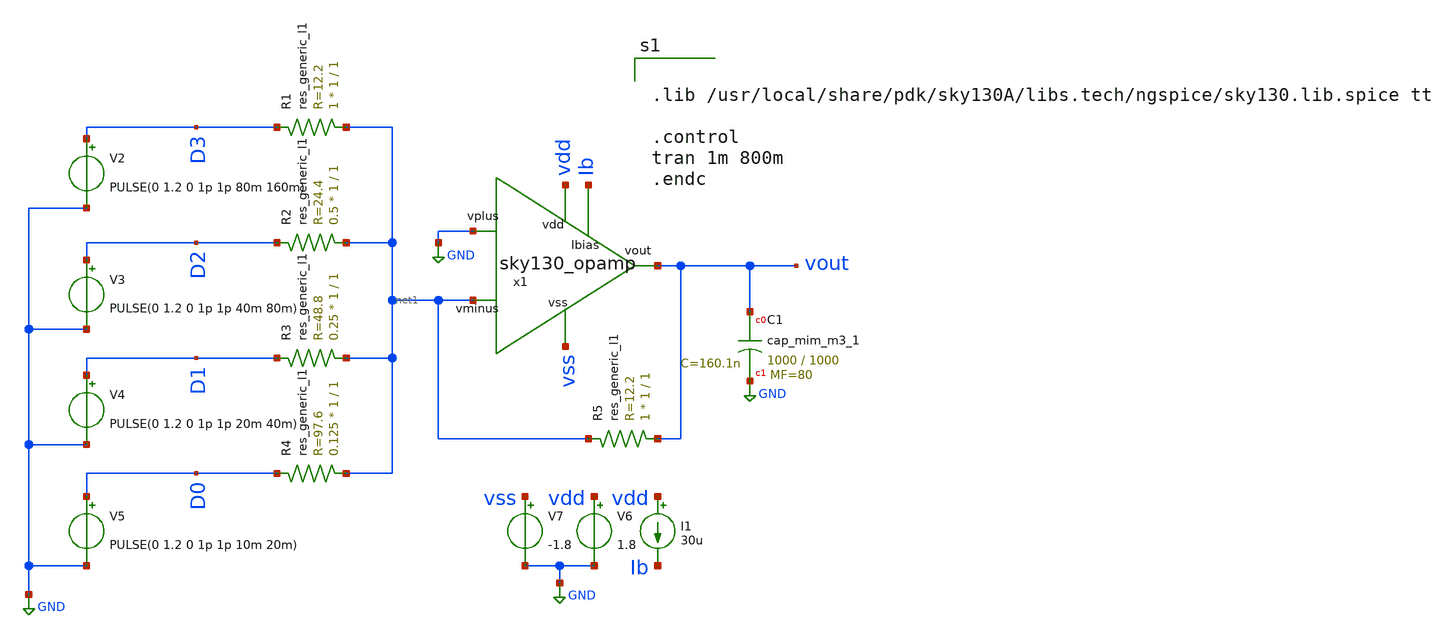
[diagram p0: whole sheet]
** sch_path: Digital to Analog Converter (DAC)/Binary Weighted DAC/binary_weighted_dac.sch
**.subckt binary_weighted_dac
x1 vdd vout GND net1 Ib vss sky130_opamp
R1 net1 D3 sky130_fd_pr__res_generic_l1 W=1 L=1 m=1
R2 net1 D2 sky130_fd_pr__res_generic_l1 W=1 L=1 m=0.5
R3 net1 D1 sky130_fd_pr__res_generic_l1 W=1 L=1 m=0.25
R4 net1 D0 sky130_fd_pr__res_generic_l1 W=1 L=1 m=0.125
V2 D3 GND PULSE(0 1.2 0 1p 1p 80m 160m)
V3 D2 GND PULSE(0 1.2 0 1p 1p 40m 80m)
V4 D1 GND PULSE(0 1.2 0 1p 1p 20m 40m)
V5 D0 GND PULSE(0 1.2 0 1p 1p 10m 20m)
V6 vdd GND 1.8
V7 vss GND -1.8
I1 vdd Ib 30u
R5 vout net1 sky130_fd_pr__res_generic_l1 W=1 L=1 m=1
XC1 vout GND sky130_fd_pr__cap_mim_m3_1 W=1000 L=1000 MF=80 m=80
**** begin user architecture code


.lib /usr/local/share/pdk/sky130A/libs.tech/ngspice/sky130.lib.spice tt

.control
tran 1m 800m
.endc


**** end user architecture code
**.ends

* expanding   symbol:  /home/rachtih/ADC trials/opamp/sky130_opamp.sym # of pins=6
** sym_path: Primitives/Operational Amplifier/Xschem Files/sky130_opamp.sym
** sch_path: Primitives/Operational Amplifier/Xschem Files/sky130_opamp.sch
.subckt sky130_opamp vdd vout vplus vminus Ibias vss
*.ipin Ibias
*.ipin vminus
*.ipin vplus
*.ipin vss
*.ipin vdd
*.opin vout
XM1 Ibias Ibias vss vss sky130_fd_pr__nfet_01v8 L=0.15 W=1 nf=1 ad='int((1 + 1)/2) * 1 / 1 * 0.29' as='int((1 + 2)/2) * 1 / 1 * 0.29'
+ pd='2*int((1 + 1)/2) * (1 / 1 + 0.29)' ps='2*int((1 + 2)/2) * (1 / 1 + 0.29)' nrd='0.29 / 1 ' nrs='0.29 / 1 '
+ sa=0 sb=0 sd=0 mult=1 m=1
XM2 net3 Ibias vss vss sky130_fd_pr__nfet_01v8 L=0.15 W=1 nf=1 ad='int((1 + 1)/2) * 1 / 1 * 0.29' as='int((1 + 2)/2) * 1 / 1 * 0.29'
+ pd='2*int((1 + 1)/2) * (1 / 1 + 0.29)' ps='2*int((1 + 2)/2) * (1 / 1 + 0.29)' nrd='0.29 / 1 ' nrs='0.29 / 1 '
+ sa=0 sb=0 sd=0 mult=1 m=1
XM3 net1 vminus net3 vss sky130_fd_pr__nfet_01v8 L=0.15 W=1 nf=1 ad='int((1 + 1)/2) * 1 / 1 * 0.29' as='int((1 + 2)/2) * 1 / 1 * 0.29'
+ pd='2*int((1 + 1)/2) * (1 / 1 + 0.29)' ps='2*int((1 + 2)/2) * (1 / 1 + 0.29)' nrd='0.29 / 1 ' nrs='0.29 / 1 '
+ sa=0 sb=0 sd=0 mult=1 m=1
XM4 net2 vplus net3 vss sky130_fd_pr__nfet_01v8 L=0.15 W=1 nf=1 ad='int((1 + 1)/2) * 1 / 1 * 0.29' as='int((1 + 2)/2) * 1 / 1 * 0.29'
+ pd='2*int((1 + 1)/2) * (1 / 1 + 0.29)' ps='2*int((1 + 2)/2) * (1 / 1 + 0.29)' nrd='0.29 / 1 ' nrs='0.29 / 1 '
+ sa=0 sb=0 sd=0 mult=1 m=1
XM5 vout Ibias vss vss sky130_fd_pr__nfet_01v8 L=0.15 W=1 nf=1 ad='int((1 + 1)/2) * 1 / 1 * 0.29' as='int((1 + 2)/2) * 1 / 1 * 0.29'
+ pd='2*int((1 + 1)/2) * (1 / 1 + 0.29)' ps='2*int((1 + 2)/2) * (1 / 1 + 0.29)' nrd='0.29 / 1 ' nrs='0.29 / 1 '
+ sa=0 sb=0 sd=0 mult=1 m=1
XM6 net2 net1 vdd vdd sky130_fd_pr__pfet_01v8 L=0.15 W=1 nf=1 ad='int((1 + 1)/2) * 1 / 1 * 0.29' as='int((1 + 2)/2) * 1 / 1 * 0.29'
+ pd='2*int((1 + 1)/2) * (1 / 1 + 0.29)' ps='2*int((1 + 2)/2) * (1 / 1 + 0.29)' nrd='0.29 / 1 ' nrs='0.29 / 1 '
+ sa=0 sb=0 sd=0 mult=1 m=1
XM7 net1 net1 vdd vdd sky130_fd_pr__pfet_01v8 L=0.15 W=1 nf=1 ad='int((1 + 1)/2) * 1 / 1 * 0.29' as='int((1 + 2)/2) * 1 / 1 * 0.29'
+ pd='2*int((1 + 1)/2) * (1 / 1 + 0.29)' ps='2*int((1 + 2)/2) * (1 / 1 + 0.29)' nrd='0.29 / 1 ' nrs='0.29 / 1 '
+ sa=0 sb=0 sd=0 mult=1 m=1
XM8 vout net2 vdd vdd sky130_fd_pr__pfet_01v8 L=0.15 W=1 nf=1 ad='int((1 + 1)/2) * 1 / 1 * 0.29' as='int((1 + 2)/2) * 1 / 1 * 0.29'
+ pd='2*int((1 + 1)/2) * (1 / 1 + 0.29)' ps='2*int((1 + 2)/2) * (1 / 1 + 0.29)' nrd='0.29 / 1 ' nrs='0.29 / 1 '
+ sa=0 sb=0 sd=0 mult=1 m=1
C1 net4 vout 2.7p m=1
R1 net2 net4 50 m=1
.ends

.GLOBAL GND
.end
